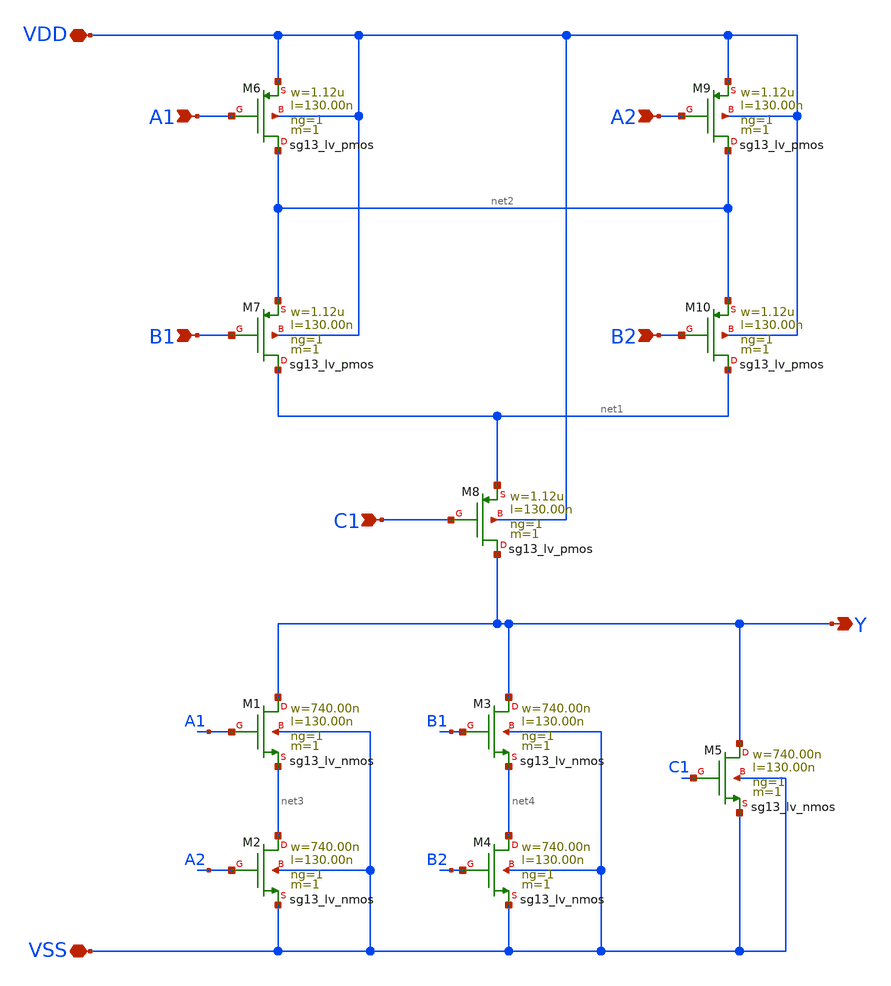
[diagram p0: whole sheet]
** sch_path: ihp-sg13g2/libs.tech/xschem/sg13g2_stdcells/sg13g2_a221oi_1.sch
**.subckt sg13g2_a221oi_1 A1 A2 B1 Y B2 C1 VDD VSS
*.ipin A1
*.ipin A2
*.ipin B1
*.opin Y
*.ipin B2
*.ipin C1
*.iopin VDD
*.iopin VSS
XM1 Y A1 net3 VSS sg13_lv_nmos w=740.00n l=130.00n ng=1 m=1 mm_ok=1
XM2 net3 A2 VSS VSS sg13_lv_nmos w=740.00n l=130.00n ng=1 m=1 mm_ok=1
XM3 Y B1 net4 VSS sg13_lv_nmos w=740.00n l=130.00n ng=1 m=1 mm_ok=1
XM4 net4 B2 VSS VSS sg13_lv_nmos w=740.00n l=130.00n ng=1 m=1 mm_ok=1
XM5 Y C1 VSS VSS sg13_lv_nmos w=740.00n l=130.00n ng=1 m=1 mm_ok=1
XM6 net2 A1 VDD VDD sg13_lv_pmos w=1.12u l=130.00n ng=1 m=1 mm_ok=1
XM7 net1 B1 net2 VDD sg13_lv_pmos w=1.12u l=130.00n ng=1 m=1 mm_ok=1
XM8 Y C1 net1 VDD sg13_lv_pmos w=1.12u l=130.00n ng=1 m=1 mm_ok=1
XM9 net2 A2 VDD VDD sg13_lv_pmos w=1.12u l=130.00n ng=1 m=1 mm_ok=1
XM10 net1 B2 net2 VDD sg13_lv_pmos w=1.12u l=130.00n ng=1 m=1 mm_ok=1
**.ends
.end
